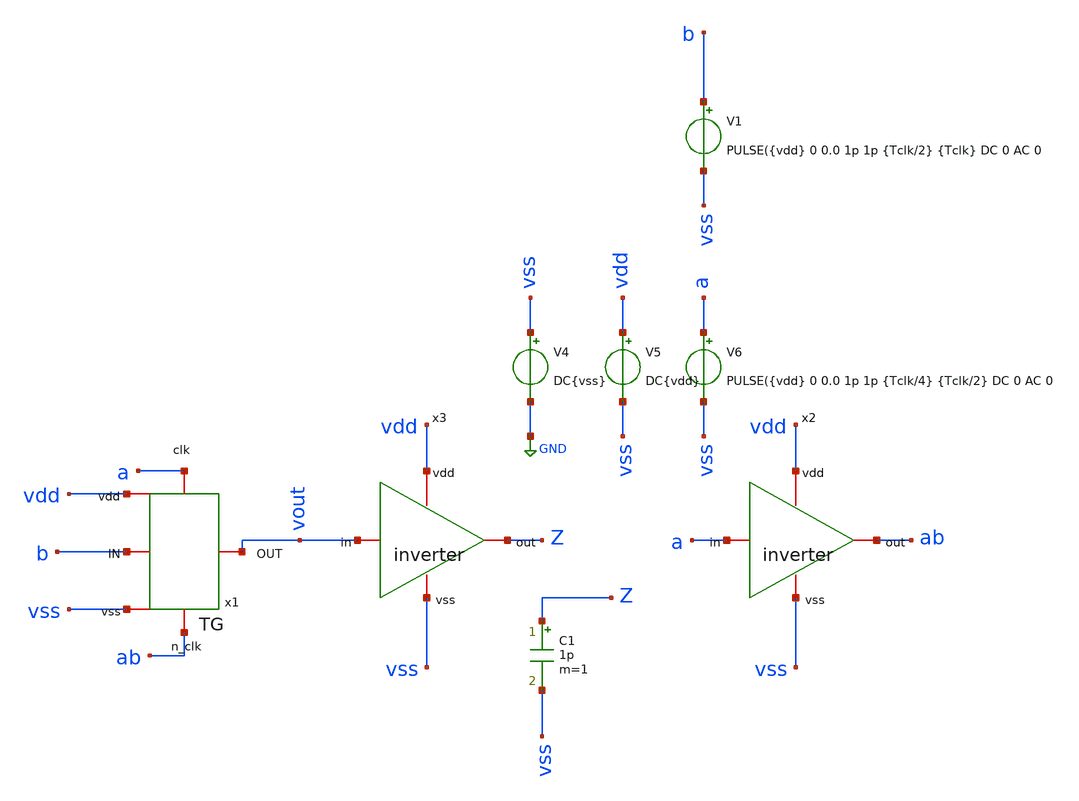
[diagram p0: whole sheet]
** sch_path: tstbnch/tg_test.sch
**.subckt tg_test
V4 vss GND DC{vss}
V5 vdd vss DC{vdd}
V6 a vss PULSE({vdd} 0 0.0 1p 1p {Tclk/4} {Tclk/2} DC 0 AC 0
C1 Z vss 1p m=1
V1 b vss PULSE({vdd} 0 0.0 1p 1p {Tclk/2} {Tclk} DC 0 AC 0
x2 vdd a ab vss inverter
x3 vdd vout Z vss inverter
x1 a vdd vss b vout ab TG
**** begin user architecture code


* Circuit Parameters
.param vdd = 1.8
.param vss = 0.0
.param Tclk = 20n
.options TEMP = 65.0
* Include Models
.lib /foss/pdks/sky130A/libs.tech/ngspice/sky130.lib.spice TT
* OP Parameters & Singals to save
.save all



*Simulations

.control

tran 0.01u 100n
setplot tran1
plot v(a) v(b)+2 v(vout)+4
reset

set filetype = ascii
write dcsweep.raw
.endc
.end


**** end user architecture code
**.ends

* expanding   symbol:  /foss/designs/sch/inverter.sym # of pins=4
** sym_path: sch/inverter.sym
** sch_path: sch/inverter.sch
.subckt inverter vdd in out vss
*.iopin out
*.iopin vdd
*.iopin vss
*.iopin in
XM1 out in vss vss sky130_fd_pr__nfet_01v8 L=0.15 W=0.45 nf=1 ad='int((nf+1)/2) * W/nf * 0.29' as='int((nf+2)/2) * W/nf * 0.29'
+ pd='2*int((nf+1)/2) * (W/nf + 0.29)' ps='2*int((nf+2)/2) * (W/nf + 0.29)' nrd='0.29 / W' nrs='0.29 / W'
+ sa=0 sb=0 sd=0 mult=1 m=1
XM2 out in vdd vdd sky130_fd_pr__pfet_01v8 L=0.15 W=0.45 nf=1 ad='int((nf+1)/2) * W/nf * 0.29' as='int((nf+2)/2) * W/nf * 0.29'
+ pd='2*int((nf+1)/2) * (W/nf + 0.29)' ps='2*int((nf+2)/2) * (W/nf + 0.29)' nrd='0.29 / W' nrs='0.29 / W'
+ sa=0 sb=0 sd=0 mult=1 m=1
.ends


* expanding   symbol:  /foss/designs/sch/TG.sym # of pins=6
** sym_path: sch/TG.sym
** sch_path: sch/TG.sch
.subckt TG clk vdd vss IN OUT n_clk
*.iopin OUT
*.iopin IN
*.iopin clk
*.iopin n_clk
*.iopin vdd
*.iopin vss
XM1 OUT clk IN vss sky130_fd_pr__nfet_01v8 L=0.15 W=0.75 nf=1 ad='int((nf+1)/2) * W/nf * 0.29' as='int((nf+2)/2) * W/nf * 0.29'
+ pd='2*int((nf+1)/2) * (W/nf + 0.29)' ps='2*int((nf+2)/2) * (W/nf + 0.29)' nrd='0.29 / W' nrs='0.29 / W'
+ sa=0 sb=0 sd=0 mult=1 m=1
XM2 OUT n_clk IN vdd sky130_fd_pr__pfet_01v8 L=0.15 W=1.5 nf=1 ad='int((nf+1)/2) * W/nf * 0.29' as='int((nf+2)/2) * W/nf * 0.29'
+ pd='2*int((nf+1)/2) * (W/nf + 0.29)' ps='2*int((nf+2)/2) * (W/nf + 0.29)' nrd='0.29 / W' nrs='0.29 / W'
+ sa=0 sb=0 sd=0 mult=1 m=1
.ends

.GLOBAL GND
.end
